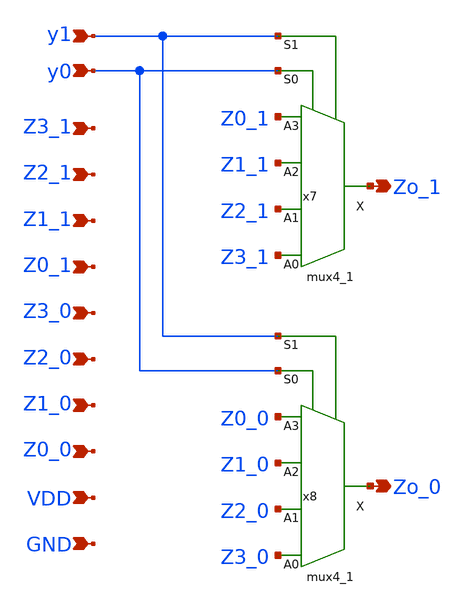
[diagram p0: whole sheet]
** sch_path: ZMUX4.sch
**.subckt ZMUX4 Z0_0 Z1_0 y0 Z2_0 Z3_0 Z0_1 Z1_1 Z2_1 Z3_1 Zo_1 Zo_0 y1 VDD GND
*.ipin Z0_0
*.ipin Z1_0
*.ipin y0
*.ipin Z2_0
*.ipin Z3_0
*.ipin Z0_1
*.ipin Z1_1
*.ipin Z2_1
*.ipin Z3_1
*.opin Zo_1
*.opin Zo_0
*.ipin y1
*.ipin VDD
*.ipin GND
x7 Z3_1 Z2_1 Z1_1 Z0_1 y0 y1 GND GND VDD VDD Zo_1 sky130_fd_sc_hd__mux4_1
x8 Z3_0 Z2_0 Z1_0 Z0_0 y0 y1 GND GND VDD VDD Zo_0 sky130_fd_sc_hd__mux4_1
**.ends
.end
